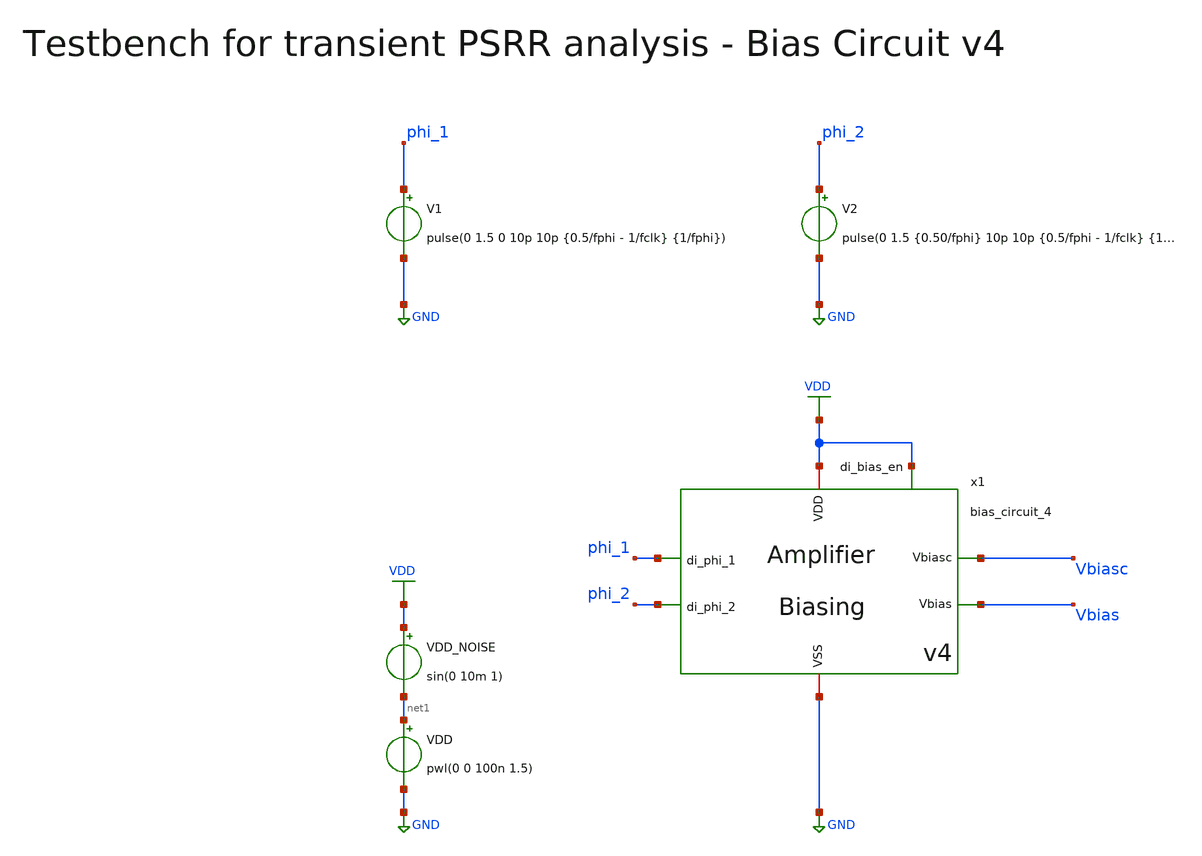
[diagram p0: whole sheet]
** sch_path: SG13G2_ATBS-ADC-main/xschem/bio_amplifier/amplifier_core/bias_circuit/bias_circuit_4/testbenches/bias_circuit_4_tb_PSRR_tran.sch
**.subckt bias_circuit_4_tb_PSRR_tran
x1 phi_2 phi_1 VDD GND Vbiasc Vbias VDD bias_circuit_4
V1 phi_1 GND pulse(0 1.5 0 10p 10p {0.5/fphi - 1/fclk} {1/fphi})
V2 phi_2 GND pulse(0 1.5 {0.50/fphi} 10p 10p {0.5/fphi - 1/fclk} {1/fphi})
VDD_NOISE VDD net1 sin(0 10m 1)
VDD net1 GND pwl(0 0 100n 1.5)
**** begin user architecture code

.lib cornerMOSlv.lib mos_tt
.lib cornerRES.lib res_typ



.param fclk=8000000
.param fphi=62500
.csparam fclk=fclk
.options klu method=gear reltol=1e-2 abstol=1e-15 gmin=1e-15
.control

* save all
save v(VDD) v(Vbias) v(Vbiasc)

setplot const

set wr_vecnames
set wr_singlescale

* User constants
* Wait until Vbias has settled.
let tstart = 500u
let fstart = 10k
let fstop = 10k
let amount_of_periods = 2
let points_per_period = 10
let points_per_dec = 1
let vamp = 0.01

* Generate a logarithmic frequency vector
compose freq_vec dec=$&const.points_per_dec start=$&const.fstart stop=$&const.fstop

* Generate PSRR vector
let PSRR_vec = freq_vec

* Loop index
let idx = 0

* For-Loop
foreach freq_val $&freq_vec
  * 10 data points per period
  * let tstep = 1/($&const.points_per_period*$freq_val)
  let tstep = 1/fclk

  * 2 periods long
  let tstop = ($&const.amount_of_periods * 1/$freq_val) + $&const.tstart

  * Alter input sine frequency
  alter @VDD_NOISE[SIN] = [ 0 $&const.vamp $freq_val 0 0 0 ]

  * Transient Analysis
  tran $&tstep $&tstop $&tstart
  write bias_circuit_4_tb_PSRR_tran.raw
  set appendwrite

  * Measurement
  * Measure maximum voltage of input
  meas tran vdd_peak_peak PP v(VDD) from=$&tstart to=$&tstop
  let vdd_peak = vdd_peak_peak / 2

  * Measure maximum voltage of output
  meas tran vbias_peak_peak PP v(Vbias) from=$&tstart to=$&tstop
  let vbias_peak = vbias_peak_peak / 2

  * Calculate PSRR
  let PSRR = vdd_peak / vbias_peak
  let PSRR_dB = vdb(PSRR)

  * Append to vector
  let const.PSRR_vec[const.idx] = PSRR_dB

  * Update index
  let const.idx = const.idx + 1
  echo ======================================================
end

print const.PSRR_vec

* Setscale for plot against frequency
setscale const.PSRR_vec const.freq_vec

* Plot PSRR vs. frequency
plot xlog const.PSRR_vec title 'PSRR' ylabel 'dB'

* Write Data
wrdata
+ /foss/designs/SG13G2_ATBS-ADC-main/python/plot_simulations/data/bias_circuit_4_tb_PSRR_tran.txt v(const.freq_vec) v(const.PSRR_vec)

*quit
.endc

**** end user architecture code
**.ends
.GLOBAL GND
.GLOBAL VDD
.end
